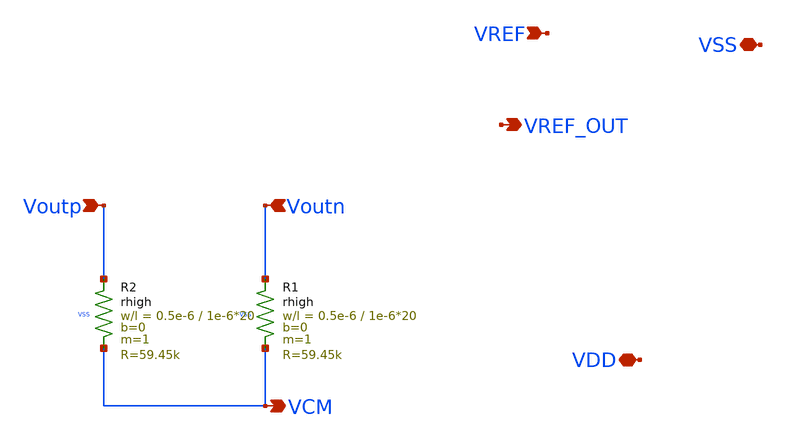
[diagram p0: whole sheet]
** sch_path: schema/ota_cmfb_cm_sense/ota_cmfb_cm_sense.sch
**.subckt ota_cmfb_cm_sense Voutp Voutn VCM VDD VSS VREF VREF_OUT
*.ipin Voutp
*.ipin Voutn
*.opin VCM
*.iopin VDD
*.iopin VSS
*.ipin VREF
*.opin VREF_OUT
XR1 Voutn VCM VSS rhigh w=0.5e-6 l=1e-6*20 m=1 b=0 mm_ok=1
XR2 Voutp VCM VSS rhigh w=0.5e-6 l=1e-6*20 m=1 b=0 mm_ok=1
**.ends
.end
